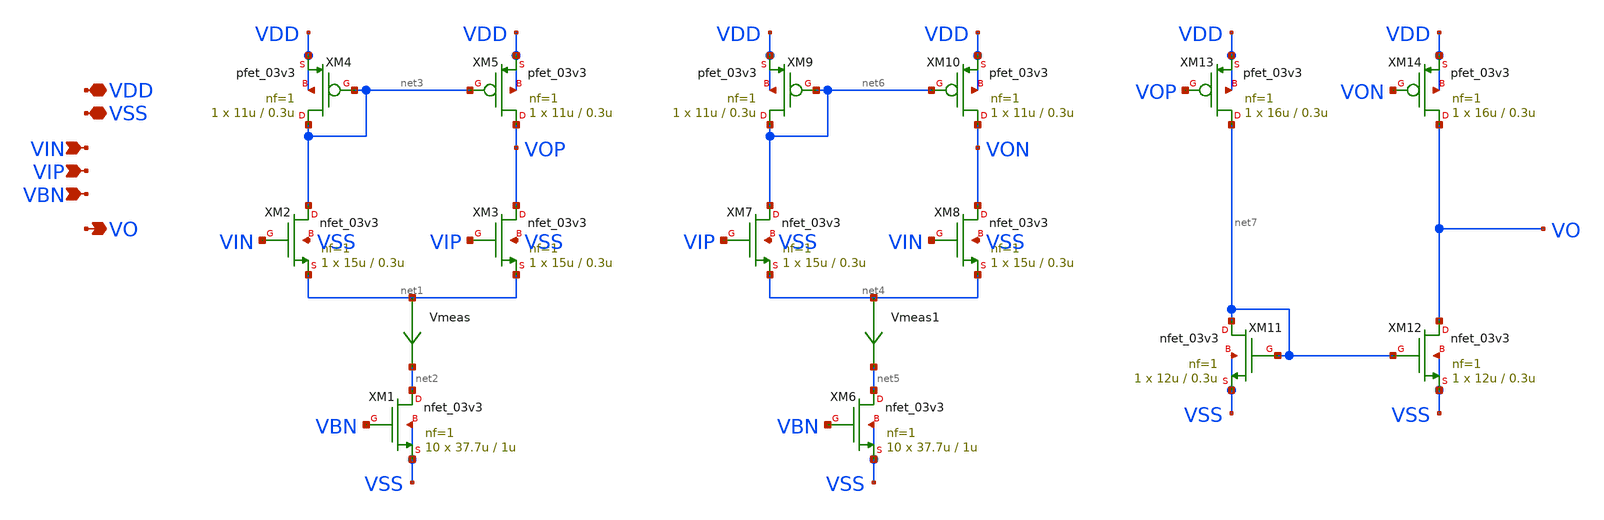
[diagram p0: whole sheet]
** sch_path: designs/libs/core_analog/d2s_converter/d2s_converter.sch
**.subckt d2s_converter VDD VSS VIN VIP VO VBN
*.iopin VDD
*.iopin VSS
*.ipin VIN
*.ipin VIP
*.opin VO
*.ipin VBN
XM1 net2 VBN VSS VSS nfet_03v3 L=1u W=37.7u nf=1 ad='int((nf+1)/2) * W/nf * 0.18u' as='int((nf+2)/2) * W/nf * 0.18u'
+ pd='2*int((nf+1)/2) * (W/nf + 0.18u)' ps='2*int((nf+2)/2) * (W/nf + 0.18u)' nrd='0.18u / W' nrs='0.18u / W'
+ sa=0 sb=0 sd=0 m=10
XM2 net3 VIN net1 VSS nfet_03v3 L=0.3u W=15u nf=1 ad='int((nf+1)/2) * W/nf * 0.18u' as='int((nf+2)/2) * W/nf * 0.18u'
+ pd='2*int((nf+1)/2) * (W/nf + 0.18u)' ps='2*int((nf+2)/2) * (W/nf + 0.18u)' nrd='0.18u / W' nrs='0.18u / W'
+ sa=0 sb=0 sd=0 m=1
XM3 VOP VIP net1 VSS nfet_03v3 L=0.3u W=15u nf=1 ad='int((nf+1)/2) * W/nf * 0.18u' as='int((nf+2)/2) * W/nf * 0.18u'
+ pd='2*int((nf+1)/2) * (W/nf + 0.18u)' ps='2*int((nf+2)/2) * (W/nf + 0.18u)' nrd='0.18u / W' nrs='0.18u / W'
+ sa=0 sb=0 sd=0 m=1
XM4 net3 net3 VDD VDD pfet_03v3 L=0.3u W=11u nf=1 ad='int((nf+1)/2) * W/nf * 0.18u' as='int((nf+2)/2) * W/nf * 0.18u'
+ pd='2*int((nf+1)/2) * (W/nf + 0.18u)' ps='2*int((nf+2)/2) * (W/nf + 0.18u)' nrd='0.18u / W' nrs='0.18u / W'
+ sa=0 sb=0 sd=0 m=1
XM5 VOP net3 VDD VDD pfet_03v3 L=0.3u W=11u nf=1 ad='int((nf+1)/2) * W/nf * 0.18u' as='int((nf+2)/2) * W/nf * 0.18u'
+ pd='2*int((nf+1)/2) * (W/nf + 0.18u)' ps='2*int((nf+2)/2) * (W/nf + 0.18u)' nrd='0.18u / W' nrs='0.18u / W'
+ sa=0 sb=0 sd=0 m=1
XM7 net6 VIP net4 VSS nfet_03v3 L=0.3u W=15u nf=1 ad='int((nf+1)/2) * W/nf * 0.18u' as='int((nf+2)/2) * W/nf * 0.18u'
+ pd='2*int((nf+1)/2) * (W/nf + 0.18u)' ps='2*int((nf+2)/2) * (W/nf + 0.18u)' nrd='0.18u / W' nrs='0.18u / W'
+ sa=0 sb=0 sd=0 m=1
XM8 VON VIN net4 VSS nfet_03v3 L=0.3u W=15u nf=1 ad='int((nf+1)/2) * W/nf * 0.18u' as='int((nf+2)/2) * W/nf * 0.18u'
+ pd='2*int((nf+1)/2) * (W/nf + 0.18u)' ps='2*int((nf+2)/2) * (W/nf + 0.18u)' nrd='0.18u / W' nrs='0.18u / W'
+ sa=0 sb=0 sd=0 m=1
XM9 net6 net6 VDD VDD pfet_03v3 L=0.3u W=11u nf=1 ad='int((nf+1)/2) * W/nf * 0.18u' as='int((nf+2)/2) * W/nf * 0.18u'
+ pd='2*int((nf+1)/2) * (W/nf + 0.18u)' ps='2*int((nf+2)/2) * (W/nf + 0.18u)' nrd='0.18u / W' nrs='0.18u / W'
+ sa=0 sb=0 sd=0 m=1
XM10 VON net6 VDD VDD pfet_03v3 L=0.3u W=11u nf=1 ad='int((nf+1)/2) * W/nf * 0.18u' as='int((nf+2)/2) * W/nf * 0.18u'
+ pd='2*int((nf+1)/2) * (W/nf + 0.18u)' ps='2*int((nf+2)/2) * (W/nf + 0.18u)' nrd='0.18u / W' nrs='0.18u / W'
+ sa=0 sb=0 sd=0 m=1
XM11 net7 net7 VSS VSS nfet_03v3 L=0.3u W=12u nf=1 ad='int((nf+1)/2) * W/nf * 0.18u' as='int((nf+2)/2) * W/nf * 0.18u'
+ pd='2*int((nf+1)/2) * (W/nf + 0.18u)' ps='2*int((nf+2)/2) * (W/nf + 0.18u)' nrd='0.18u / W' nrs='0.18u / W'
+ sa=0 sb=0 sd=0 m=1
XM12 VO net7 VSS VSS nfet_03v3 L=0.3u W=12u nf=1 ad='int((nf+1)/2) * W/nf * 0.18u' as='int((nf+2)/2) * W/nf * 0.18u'
+ pd='2*int((nf+1)/2) * (W/nf + 0.18u)' ps='2*int((nf+2)/2) * (W/nf + 0.18u)' nrd='0.18u / W' nrs='0.18u / W'
+ sa=0 sb=0 sd=0 m=1
XM13 net7 VOP VDD VDD pfet_03v3 L=0.3u W=16u nf=1 ad='int((nf+1)/2) * W/nf * 0.18u' as='int((nf+2)/2) * W/nf * 0.18u'
+ pd='2*int((nf+1)/2) * (W/nf + 0.18u)' ps='2*int((nf+2)/2) * (W/nf + 0.18u)' nrd='0.18u / W' nrs='0.18u / W'
+ sa=0 sb=0 sd=0 m=1
XM14 VO VON VDD VDD pfet_03v3 L=0.3u W=16u nf=1 ad='int((nf+1)/2) * W/nf * 0.18u' as='int((nf+2)/2) * W/nf * 0.18u'
+ pd='2*int((nf+1)/2) * (W/nf + 0.18u)' ps='2*int((nf+2)/2) * (W/nf + 0.18u)' nrd='0.18u / W' nrs='0.18u / W'
+ sa=0 sb=0 sd=0 m=1
Vmeas net1 net2 0
.save i(vmeas)
Vmeas1 net4 net5 0
.save i(vmeas1)
XM6 net5 VBN VSS VSS nfet_03v3 L=1u W=37.7u nf=1 ad='int((nf+1)/2) * W/nf * 0.18u' as='int((nf+2)/2) * W/nf * 0.18u'
+ pd='2*int((nf+1)/2) * (W/nf + 0.18u)' ps='2*int((nf+2)/2) * (W/nf + 0.18u)' nrd='0.18u / W' nrs='0.18u / W'
+ sa=0 sb=0 sd=0 m=10
**.ends
.end
